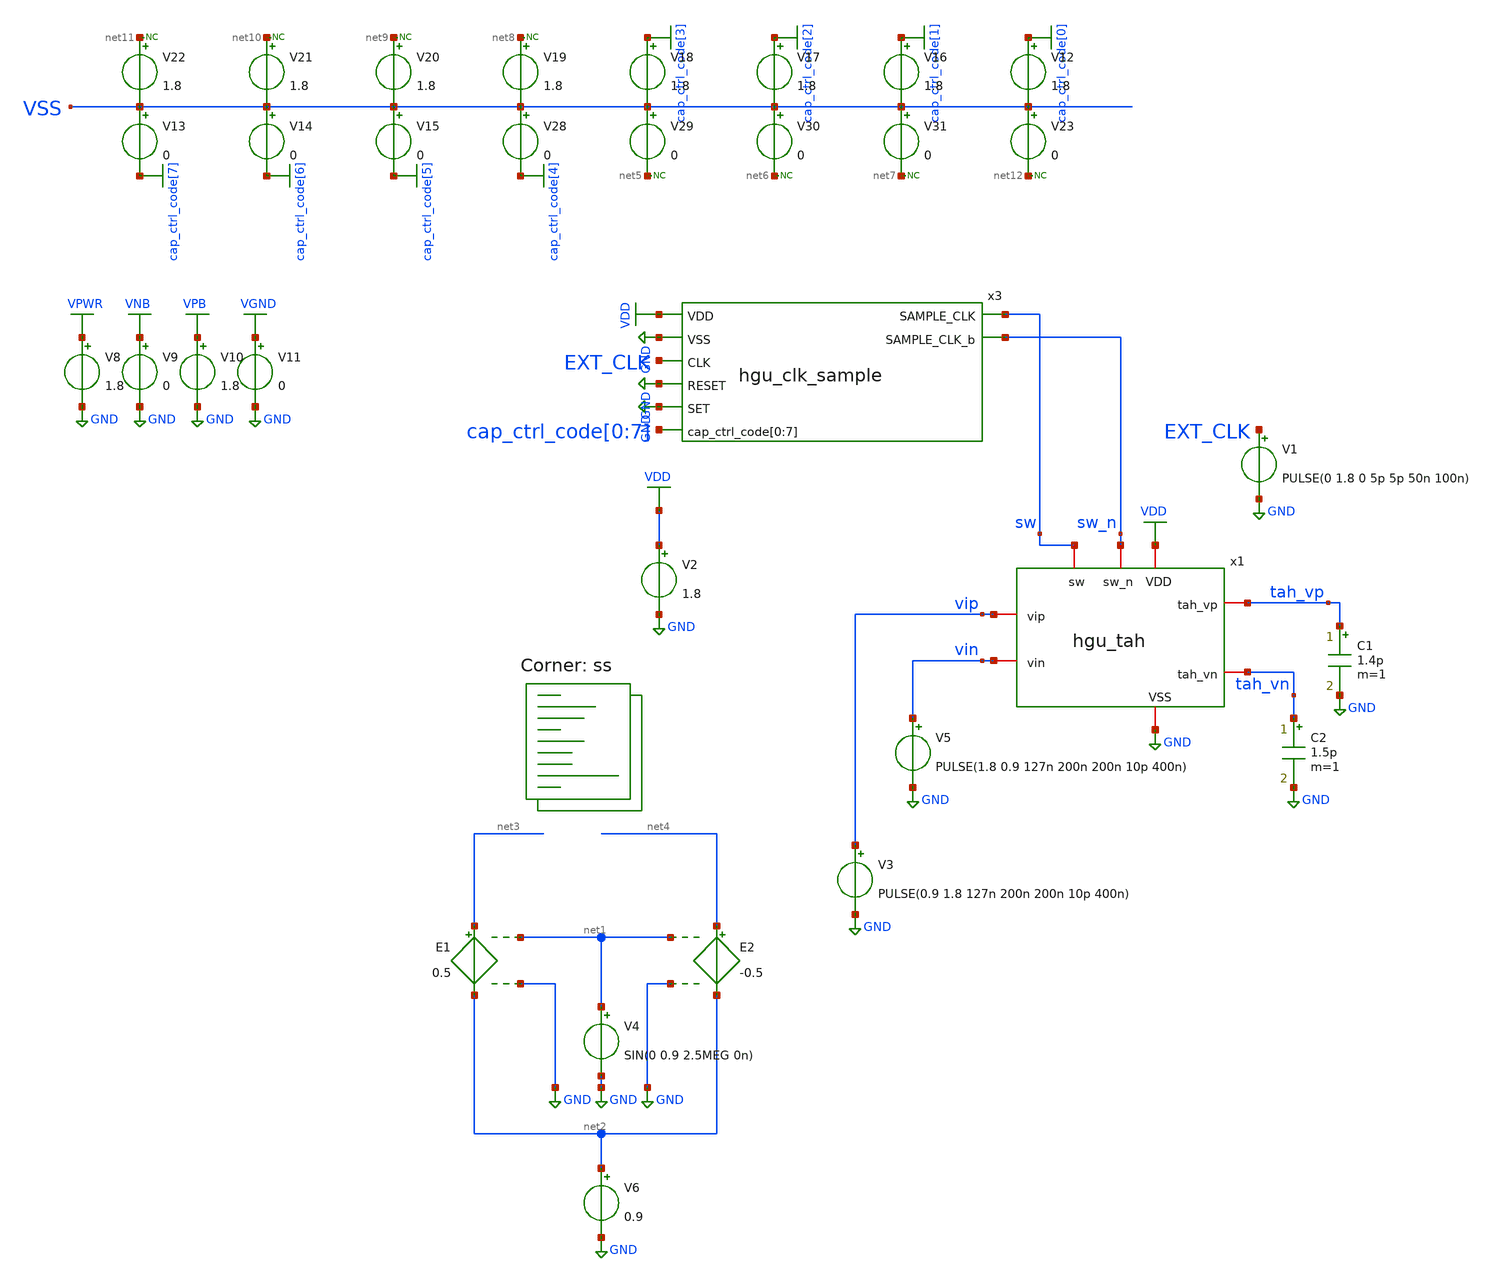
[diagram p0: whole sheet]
** sch_path: hgu/tb/tb_hgu_tah_nonideal.sch
**.subckt tb_hgu_tah_nonideal
x1 sw VDD GND sw_n tah_vp vip vin tah_vn hgu_tah
V2 VDD GND 1.8
C2 tah_vn GND 1.5p m=1
C1 tah_vp GND 1.4p m=1
V1 EXT_CLK GND PULSE(0 1.8 0 5p 5p 50n 100n)
V4 net1 GND SIN(0 0.9 2.5MEG 0n)
E1 net3 net2 net1 GND 0.5
E2 net4 net2 net1 GND -0.5
V6 net2 GND 0.9
x3 sw VDD GND EXT_CLK GND GND sw_n cap_ctrl_code[0] cap_ctrl_code[1] cap_ctrl_code[2]
+ cap_ctrl_code[3] cap_ctrl_code[4] cap_ctrl_code[5] cap_ctrl_code[6] cap_ctrl_code[7] hgu_clk_sample
V12 cap_ctrl_code[0] VSS 1.8
V13 VSS cap_ctrl_code[7] 0
V14 VSS cap_ctrl_code[6] 0
V15 VSS cap_ctrl_code[5] 0
V28 VSS cap_ctrl_code[4] 0
V29 VSS net5 0
V30 VSS net6 0
V31 VSS net7 0
V16 cap_ctrl_code[1] VSS 1.8
V17 cap_ctrl_code[2] VSS 1.8
V18 cap_ctrl_code[3] VSS 1.8
V19 net8 VSS 1.8
V20 net9 VSS 1.8
V21 net10 VSS 1.8
V22 net11 VSS 1.8
V23 VSS net12 0
* noconn #net11
* noconn #net10
* noconn #net9
* noconn #net8
* noconn #net5
* noconn #net6
* noconn #net7
* noconn #net12
V8 VPWR GND 1.8
V9 VNB GND 0
V10 VPB GND 1.8
V11 VGND GND 0
V3 vip GND PULSE(0.9 1.8 127n 200n 200n 10p 400n)
V5 vin GND PULSE(1.8 0.9 127n 200n 200n 10p 400n)
**** begin user architecture code


.save all
.temp = 25
.tran 100p 600n
.OPTIONS savecurrents
.include /foss/pdks/sky130A/libs.ref/sky130_fd_sc_hd/spice/sky130_fd_sc_hd.spice

.control
run
	plot v(sw)-0.9 v(sw_n)-0.9 tah_vp-tah_vn vip-vin
        let svdd = 1.8
        let max = svdd*0.8
        let min = svdd*0.2
        let mid = svdd*0.5
	let input = vip-vin
        meas tran rising_s find time when V(tah_vp-tah_vn)=min RISE=1 TD=100n
        meas tran rising_e find time when V(tah_vp-tah_vn)=max RISE=1 TD=100n
        let rising_time = rising_e-rising_s
        meas tran falling_s find time when V(tah_vp-tah_vn)=max FALL=1 TD=1000p
        meas tran falling_e find time when V(tah_vp-tah_vn)=min FALL=1 TD=1000p
        let falling_time = falling_e-falling_s
        meas tran IN find time when V(sw)=mid RISE=1 TD=350n
        meas tran OUT find time when V(tah_vp-tah_vn)=mid RISE=1 TD=350n
        let rising_delay = OUT-IN
        meas tran fIN find time when V(sw)=mid RISE=1 TD=100n
        meas tran fOUT find time when V(tah_vp-tah_vn)=mid FALL=1 TD=100n
        let falling_delay = fOUT-fIN
	meas tran holdval find input when V(sw)=mid FALL=1 TD=300n


        print holdval

*plot v(sw)+2 v(sw) tah_vp tah_vn+2
*plot v(sw) tah_vp-tah_vn vip-vin
.endc


.lib $::SKYWATER_MODELS/sky130.lib.spice ss
**** end user architecture code
**.ends

* expanding   symbol:  ../xschem/hgu_clk_sample.sym # of pins=8
** sym_path: hgu/xschem/hgu_clk_sample.sym
** sch_path: hgu/xschem/hgu_clk_sample.sch
.subckt hgu_clk_sample SAMPLE_CLK VDD VSS CLK RESET SET SAMPLE_CLK_b cap_ctrl_code[0]
+ cap_ctrl_code[1] cap_ctrl_code[2] cap_ctrl_code[3] cap_ctrl_code[4] cap_ctrl_code[5] cap_ctrl_code[6]
+ cap_ctrl_code[7]
*.ipin VDD
*.ipin VSS
*.ipin SET
*.ipin RESET
*.ipin CLK
*.ipin
*+ cap_ctrl_code[0],cap_ctrl_code[1],cap_ctrl_code[2],cap_ctrl_code[3],cap_ctrl_code[4],cap_ctrl_code[5],cap_ctrl_code[6],cap_ctrl_code[7]
*.opin SAMPLE_CLK
*.opin SAMPLE_CLK_b
x1 net2 CLK RESET SET hgu_clk_div
x2 VDD net2 net8 VSS cap_ctrl_code[0] cap_ctrl_code[1] cap_ctrl_code[2] cap_ctrl_code[3]
+ cap_ctrl_code[4] cap_ctrl_code[5] cap_ctrl_code[6] cap_ctrl_code[7] hgu_delay DELAY_CAP=8f
x7 net8 VGND VNB VPB VPWR net1 sky130_fd_sc_hd__inv_1
C1 net1 VSS 5f m=1
C2 net2 VSS 5f m=1
C3 net8 VSS 5f m=1
x3 net2 net1 VGND VNB VPB VPWR net4 sky130_fd_sc_hd__nand2_1
XM7 net7 net3 VSS VSS sky130_fd_pr__nfet_01v8 L=0.15 W=0.42 nf=1 ad='int((nf+1)/2) * W/nf * 0.29' as='int((nf+2)/2) * W/nf * 0.29'
+ pd='2*int((nf+1)/2) * (W/nf + 0.29)' ps='2*int((nf+2)/2) * (W/nf + 0.29)' nrd='0.29 / W' nrs='0.29 / W'
+ sa=0 sb=0 sd=0 mult=1 m=1
XM8 net7 net3 VDD VDD sky130_fd_pr__pfet_01v8 L=0.15 W=1.26 nf=1 ad='int((nf+1)/2) * W/nf * 0.29' as='int((nf+2)/2) * W/nf * 0.29'
+ pd='2*int((nf+1)/2) * (W/nf + 0.29)' ps='2*int((nf+2)/2) * (W/nf + 0.29)' nrd='0.29 / W' nrs='0.29 / W'
+ sa=0 sb=0 sd=0 mult=1 m=1
XM9 net5 net4 VSS VSS sky130_fd_pr__nfet_01v8 L=0.15 W=0.42 nf=1 ad='int((nf+1)/2) * W/nf * 0.29' as='int((nf+2)/2) * W/nf * 0.29'
+ pd='2*int((nf+1)/2) * (W/nf + 0.29)' ps='2*int((nf+2)/2) * (W/nf + 0.29)' nrd='0.29 / W' nrs='0.29 / W'
+ sa=0 sb=0 sd=0 mult=1 m=1
XM10 net5 net4 VDD VDD sky130_fd_pr__pfet_01v8 L=0.15 W=1.4 nf=1 ad='int((nf+1)/2) * W/nf * 0.29' as='int((nf+2)/2) * W/nf * 0.29'
+ pd='2*int((nf+1)/2) * (W/nf + 0.29)' ps='2*int((nf+2)/2) * (W/nf + 0.29)' nrd='0.29 / W' nrs='0.29 / W'
+ sa=0 sb=0 sd=0 mult=1 m=1
XM11 net6 net5 VSS VSS sky130_fd_pr__nfet_01v8 L=0.15 W=0.42 nf=1 ad='int((nf+1)/2) * W/nf * 0.29' as='int((nf+2)/2) * W/nf * 0.29'
+ pd='2*int((nf+1)/2) * (W/nf + 0.29)' ps='2*int((nf+2)/2) * (W/nf + 0.29)' nrd='0.29 / W' nrs='0.29 / W'
+ sa=0 sb=0 sd=0 mult=1 m=1
XM12 net6 net5 VDD VDD sky130_fd_pr__pfet_01v8 L=0.15 W=1.26 nf=1 ad='int((nf+1)/2) * W/nf * 0.29' as='int((nf+2)/2) * W/nf * 0.29'
+ pd='2*int((nf+1)/2) * (W/nf + 0.29)' ps='2*int((nf+2)/2) * (W/nf + 0.29)' nrd='0.29 / W' nrs='0.29 / W'
+ sa=0 sb=0 sd=0 mult=1 m=1
XM13 net4 VSS net3 VDD sky130_fd_pr__pfet_01v8 L=0.15 W=1.9 nf=1 ad='int((nf+1)/2) * W/nf * 0.29' as='int((nf+2)/2) * W/nf * 0.29'
+ pd='2*int((nf+1)/2) * (W/nf + 0.29)' ps='2*int((nf+2)/2) * (W/nf + 0.29)' nrd='0.29 / W' nrs='0.29 / W'
+ sa=0 sb=0 sd=0 mult=1 m=1
XM14 net4 VDD net3 VSS sky130_fd_pr__nfet_01v8 L=0.15 W=0.42 nf=1 ad='int((nf+1)/2) * W/nf * 0.29' as='int((nf+2)/2) * W/nf * 0.29'
+ pd='2*int((nf+1)/2) * (W/nf + 0.29)' ps='2*int((nf+2)/2) * (W/nf + 0.29)' nrd='0.29 / W' nrs='0.29 / W'
+ sa=0 sb=0 sd=0 mult=1 m=1
XM15 SAMPLE_CLK net6 VSS VSS sky130_fd_pr__nfet_01v8 L=0.15 W='0.42 * 3 ' nf=3 ad='int((nf+1)/2) * W / nf * 0.29'
+ as='int((nf+2)/2) * W / nf * 0.29' pd='2*int((nf+1)/2) * (W / nf + 0.29)' ps='2*int((nf+2)/2) * (W / nf + 0.29)'
+ nrd='0.29 / W ' nrs='0.29 / W ' sa=0 sb=0 sd=0 mult=1 m=1
XM16 SAMPLE_CLK net6 VDD VDD sky130_fd_pr__pfet_01v8 L=0.15 W='1.26 * 3 ' nf=3 ad='int((nf+1)/2) * W / nf * 0.29'
+ as='int((nf+2)/2) * W / nf * 0.29' pd='2*int((nf+1)/2) * (W / nf + 0.29)' ps='2*int((nf+2)/2) * (W / nf + 0.29)'
+ nrd='0.29 / W ' nrs='0.29 / W ' sa=0 sb=0 sd=0 mult=1 m=1
XM17 SAMPLE_CLK_b net7 VDD VDD sky130_fd_pr__pfet_01v8 L=0.15 W='1.26 * 3 ' nf=3 ad='int((nf+1)/2) * W / nf * 0.29'
+ as='int((nf+2)/2) * W / nf * 0.29' pd='2*int((nf+1)/2) * (W / nf + 0.29)' ps='2*int((nf+2)/2) * (W / nf + 0.29)'
+ nrd='0.29 / W ' nrs='0.29 / W ' sa=0 sb=0 sd=0 mult=1 m=1
XM18 SAMPLE_CLK_b net7 VSS VSS sky130_fd_pr__nfet_01v8 L=0.15 W='0.42 * 3 ' nf=3 ad='int((nf+1)/2) * W / nf * 0.29'
+ as='int((nf+2)/2) * W / nf * 0.29' pd='2*int((nf+1)/2) * (W / nf + 0.29)' ps='2*int((nf+2)/2) * (W / nf + 0.29)'
+ nrd='0.29 / W ' nrs='0.29 / W ' sa=0 sb=0 sd=0 mult=1 m=1
.ends


* expanding   symbol:  ../xschem/hgu_clk_div.sym # of pins=4
** sym_path: hgu/xschem/hgu_clk_div.sym
** sch_path: hgu/xschem/hgu_clk_div.sch
.subckt hgu_clk_div DIV_CLK CLK RESET SET
*.opin DIV_CLK
*.ipin SET
*.ipin RESET
*.ipin CLK
x2 CLK D_loop net1 net2 VGND VNB VPB VPWR DIV_CLK D_loop sky130_fd_sc_hd__dfbbp_1
x3 SET VGND VNB VPB VPWR net2 sky130_fd_sc_hd__inv_1
x4 RESET VGND VNB VPB VPWR net1 sky130_fd_sc_hd__inv_1
.ends


* expanding   symbol:  ../xschem/hgu_delay.sym # of pins=5
** sym_path: hgu/xschem/hgu_delay.sym
** sch_path: hgu/xschem/hgu_delay.sch
.subckt hgu_delay VDD IN OUT VSS CAP_CTRL_CODE[0] CAP_CTRL_CODE[1] CAP_CTRL_CODE[2] CAP_CTRL_CODE[3]
+ CAP_CTRL_CODE[4] CAP_CTRL_CODE[5] CAP_CTRL_CODE[6] CAP_CTRL_CODE[7]  DELAY_CAP=DELAY_CAP
*.ipin IN
*.ipin VDD
*.ipin VSS
*.opin OUT
*.ipin
*+ CAP_CTRL_CODE[0],CAP_CTRL_CODE[1],CAP_CTRL_CODE[2],CAP_CTRL_CODE[3],CAP_CTRL_CODE[4],CAP_CTRL_CODE[5],CAP_CTRL_CODE[6],CAP_CTRL_CODE[7]
XM1 net1 IN VSS VSS sky130_fd_pr__nfet_01v8 L=3.69 W=0.42 nf=1 ad='int((nf+1)/2) * W/nf * 0.29' as='int((nf+2)/2) * W/nf * 0.29'
+ pd='2*int((nf+1)/2) * (W/nf + 0.29)' ps='2*int((nf+2)/2) * (W/nf + 0.29)' nrd='0.29 / W' nrs='0.29 / W'
+ sa=0 sb=0 sd=0 mult=1 m=1
XM2 net1 IN VDD VDD sky130_fd_pr__pfet_01v8 L=1.5 W=0.8 nf=1 ad='int((nf+1)/2) * W/nf * 0.29' as='int((nf+2)/2) * W/nf * 0.29'
+ pd='2*int((nf+1)/2) * (W/nf + 0.29)' ps='2*int((nf+2)/2) * (W/nf + 0.29)' nrd='0.29 / W' nrs='0.29 / W'
+ sa=0 sb=0 sd=0 mult=1 m=1
XM3 VSS net1 VSS VSS sky130_fd_pr__nfet_01v8 L=2.045 W=1.375 nf=1 ad='int((nf+1)/2) * W/nf * 0.29' as='int((nf+2)/2) * W/nf * 0.29'
+ pd='2*int((nf+1)/2) * (W/nf + 0.29)' ps='2*int((nf+2)/2) * (W/nf + 0.29)' nrd='0.29 / W' nrs='0.29 / W'
+ sa=0 sb=0 sd=0 mult=1 m=1
XM4 OUT net1 net3 VSS sky130_fd_pr__nfet_01v8 L=0.15 W=0.42 nf=1 ad='int((nf+1)/2) * W/nf * 0.29' as='int((nf+2)/2) * W/nf * 0.29'
+ pd='2*int((nf+1)/2) * (W/nf + 0.29)' ps='2*int((nf+2)/2) * (W/nf + 0.29)' nrd='0.29 / W' nrs='0.29 / W'
+ sa=0 sb=0 sd=0 mult=1 m=1
XM5 OUT net1 net2 VDD sky130_fd_pr__pfet_01v8 L=0.15 W=0.8 nf=1 ad='int((nf+1)/2) * W/nf * 0.29' as='int((nf+2)/2) * W/nf * 0.29'
+ pd='2*int((nf+1)/2) * (W/nf + 0.29)' ps='2*int((nf+2)/2) * (W/nf + 0.29)' nrd='0.29 / W' nrs='0.29 / W'
+ sa=0 sb=0 sd=0 mult=1 m=1
XM6 net3 net1 VSS VSS sky130_fd_pr__nfet_01v8 L=0.15 W=0.42 nf=1 ad='int((nf+1)/2) * W/nf * 0.29' as='int((nf+2)/2) * W/nf * 0.29'
+ pd='2*int((nf+1)/2) * (W/nf + 0.29)' ps='2*int((nf+2)/2) * (W/nf + 0.29)' nrd='0.29 / W' nrs='0.29 / W'
+ sa=0 sb=0 sd=0 mult=1 m=1
XM7 net2 net1 VDD VDD sky130_fd_pr__pfet_01v8 L=0.15 W=0.8 nf=1 ad='int((nf+1)/2) * W/nf * 0.29' as='int((nf+2)/2) * W/nf * 0.29'
+ pd='2*int((nf+1)/2) * (W/nf + 0.29)' ps='2*int((nf+2)/2) * (W/nf + 0.29)' nrd='0.29 / W' nrs='0.29 / W'
+ sa=0 sb=0 sd=0 mult=1 m=1
XM8 VDD OUT net3 VSS sky130_fd_pr__nfet_01v8 L=0.15 W=0.84 nf=1 ad='int((nf+1)/2) * W/nf * 0.29' as='int((nf+2)/2) * W/nf * 0.29'
+ pd='2*int((nf+1)/2) * (W/nf + 0.29)' ps='2*int((nf+2)/2) * (W/nf + 0.29)' nrd='0.29 / W' nrs='0.29 / W'
+ sa=0 sb=0 sd=0 mult=1 m=1
XM9 VSS OUT net2 VDD sky130_fd_pr__pfet_01v8 L=0.15 W=1.6 nf=1 ad='int((nf+1)/2) * W/nf * 0.29' as='int((nf+2)/2) * W/nf * 0.29'
+ pd='2*int((nf+1)/2) * (W/nf + 0.29)' ps='2*int((nf+2)/2) * (W/nf + 0.29)' nrd='0.29 / W' nrs='0.29 / W'
+ sa=0 sb=0 sd=0 mult=1 m=1
x2 CAP_CTRL_CODE[0] VSS net1 hgu_sw_cap DELAY_CAP=DELAY_CAP
x3[1] CAP_CTRL_CODE[1] VSS net1 hgu_sw_cap DELAY_CAP=DELAY_CAP
x3[0] CAP_CTRL_CODE[1] VSS net1 hgu_sw_cap DELAY_CAP=DELAY_CAP
x4[3] CAP_CTRL_CODE[2] VSS net1 hgu_sw_cap DELAY_CAP=DELAY_CAP
x4[2] CAP_CTRL_CODE[2] VSS net1 hgu_sw_cap DELAY_CAP=DELAY_CAP
x4[1] CAP_CTRL_CODE[2] VSS net1 hgu_sw_cap DELAY_CAP=DELAY_CAP
x4[0] CAP_CTRL_CODE[2] VSS net1 hgu_sw_cap DELAY_CAP=DELAY_CAP
x5[7] CAP_CTRL_CODE[3] VSS net1 hgu_sw_cap DELAY_CAP=DELAY_CAP
x5[6] CAP_CTRL_CODE[3] VSS net1 hgu_sw_cap DELAY_CAP=DELAY_CAP
x5[5] CAP_CTRL_CODE[3] VSS net1 hgu_sw_cap DELAY_CAP=DELAY_CAP
x5[4] CAP_CTRL_CODE[3] VSS net1 hgu_sw_cap DELAY_CAP=DELAY_CAP
x5[3] CAP_CTRL_CODE[3] VSS net1 hgu_sw_cap DELAY_CAP=DELAY_CAP
x5[2] CAP_CTRL_CODE[3] VSS net1 hgu_sw_cap DELAY_CAP=DELAY_CAP
x5[1] CAP_CTRL_CODE[3] VSS net1 hgu_sw_cap DELAY_CAP=DELAY_CAP
x5[0] CAP_CTRL_CODE[3] VSS net1 hgu_sw_cap DELAY_CAP=DELAY_CAP
x6[15] CAP_CTRL_CODE[4] VSS net1 hgu_sw_cap DELAY_CAP=DELAY_CAP
x6[14] CAP_CTRL_CODE[4] VSS net1 hgu_sw_cap DELAY_CAP=DELAY_CAP
x6[13] CAP_CTRL_CODE[4] VSS net1 hgu_sw_cap DELAY_CAP=DELAY_CAP
x6[12] CAP_CTRL_CODE[4] VSS net1 hgu_sw_cap DELAY_CAP=DELAY_CAP
x6[11] CAP_CTRL_CODE[4] VSS net1 hgu_sw_cap DELAY_CAP=DELAY_CAP
x6[10] CAP_CTRL_CODE[4] VSS net1 hgu_sw_cap DELAY_CAP=DELAY_CAP
x6[9] CAP_CTRL_CODE[4] VSS net1 hgu_sw_cap DELAY_CAP=DELAY_CAP
x6[8] CAP_CTRL_CODE[4] VSS net1 hgu_sw_cap DELAY_CAP=DELAY_CAP
x6[7] CAP_CTRL_CODE[4] VSS net1 hgu_sw_cap DELAY_CAP=DELAY_CAP
x6[6] CAP_CTRL_CODE[4] VSS net1 hgu_sw_cap DELAY_CAP=DELAY_CAP
x6[5] CAP_CTRL_CODE[4] VSS net1 hgu_sw_cap DELAY_CAP=DELAY_CAP
x6[4] CAP_CTRL_CODE[4] VSS net1 hgu_sw_cap DELAY_CAP=DELAY_CAP
x6[3] CAP_CTRL_CODE[4] VSS net1 hgu_sw_cap DELAY_CAP=DELAY_CAP
x6[2] CAP_CTRL_CODE[4] VSS net1 hgu_sw_cap DELAY_CAP=DELAY_CAP
x6[1] CAP_CTRL_CODE[4] VSS net1 hgu_sw_cap DELAY_CAP=DELAY_CAP
x6[0] CAP_CTRL_CODE[4] VSS net1 hgu_sw_cap DELAY_CAP=DELAY_CAP
x7[31] CAP_CTRL_CODE[5] VSS net1 hgu_sw_cap DELAY_CAP=DELAY_CAP
x7[30] CAP_CTRL_CODE[5] VSS net1 hgu_sw_cap DELAY_CAP=DELAY_CAP
x7[29] CAP_CTRL_CODE[5] VSS net1 hgu_sw_cap DELAY_CAP=DELAY_CAP
x7[28] CAP_CTRL_CODE[5] VSS net1 hgu_sw_cap DELAY_CAP=DELAY_CAP
x7[27] CAP_CTRL_CODE[5] VSS net1 hgu_sw_cap DELAY_CAP=DELAY_CAP
x7[26] CAP_CTRL_CODE[5] VSS net1 hgu_sw_cap DELAY_CAP=DELAY_CAP
x7[25] CAP_CTRL_CODE[5] VSS net1 hgu_sw_cap DELAY_CAP=DELAY_CAP
x7[24] CAP_CTRL_CODE[5] VSS net1 hgu_sw_cap DELAY_CAP=DELAY_CAP
x7[23] CAP_CTRL_CODE[5] VSS net1 hgu_sw_cap DELAY_CAP=DELAY_CAP
x7[22] CAP_CTRL_CODE[5] VSS net1 hgu_sw_cap DELAY_CAP=DELAY_CAP
x7[21] CAP_CTRL_CODE[5] VSS net1 hgu_sw_cap DELAY_CAP=DELAY_CAP
x7[20] CAP_CTRL_CODE[5] VSS net1 hgu_sw_cap DELAY_CAP=DELAY_CAP
x7[19] CAP_CTRL_CODE[5] VSS net1 hgu_sw_cap DELAY_CAP=DELAY_CAP
x7[18] CAP_CTRL_CODE[5] VSS net1 hgu_sw_cap DELAY_CAP=DELAY_CAP
x7[17] CAP_CTRL_CODE[5] VSS net1 hgu_sw_cap DELAY_CAP=DELAY_CAP
x7[16] CAP_CTRL_CODE[5] VSS net1 hgu_sw_cap DELAY_CAP=DELAY_CAP
x7[15] CAP_CTRL_CODE[5] VSS net1 hgu_sw_cap DELAY_CAP=DELAY_CAP
x7[14] CAP_CTRL_CODE[5] VSS net1 hgu_sw_cap DELAY_CAP=DELAY_CAP
x7[13] CAP_CTRL_CODE[5] VSS net1 hgu_sw_cap DELAY_CAP=DELAY_CAP
x7[12] CAP_CTRL_CODE[5] VSS net1 hgu_sw_cap DELAY_CAP=DELAY_CAP
x7[11] CAP_CTRL_CODE[5] VSS net1 hgu_sw_cap DELAY_CAP=DELAY_CAP
x7[10] CAP_CTRL_CODE[5] VSS net1 hgu_sw_cap DELAY_CAP=DELAY_CAP
x7[9] CAP_CTRL_CODE[5] VSS net1 hgu_sw_cap DELAY_CAP=DELAY_CAP
x7[8] CAP_CTRL_CODE[5] VSS net1 hgu_sw_cap DELAY_CAP=DELAY_CAP
x7[7] CAP_CTRL_CODE[5] VSS net1 hgu_sw_cap DELAY_CAP=DELAY_CAP
x7[6] CAP_CTRL_CODE[5] VSS net1 hgu_sw_cap DELAY_CAP=DELAY_CAP
x7[5] CAP_CTRL_CODE[5] VSS net1 hgu_sw_cap DELAY_CAP=DELAY_CAP
x7[4] CAP_CTRL_CODE[5] VSS net1 hgu_sw_cap DELAY_CAP=DELAY_CAP
x7[3] CAP_CTRL_CODE[5] VSS net1 hgu_sw_cap DELAY_CAP=DELAY_CAP
x7[2] CAP_CTRL_CODE[5] VSS net1 hgu_sw_cap DELAY_CAP=DELAY_CAP
x7[1] CAP_CTRL_CODE[5] VSS net1 hgu_sw_cap DELAY_CAP=DELAY_CAP
x7[0] CAP_CTRL_CODE[5] VSS net1 hgu_sw_cap DELAY_CAP=DELAY_CAP
x8[63] CAP_CTRL_CODE[6] VSS net1 hgu_sw_cap DELAY_CAP=DELAY_CAP
x8[62] CAP_CTRL_CODE[6] VSS net1 hgu_sw_cap DELAY_CAP=DELAY_CAP
x8[61] CAP_CTRL_CODE[6] VSS net1 hgu_sw_cap DELAY_CAP=DELAY_CAP
x8[60] CAP_CTRL_CODE[6] VSS net1 hgu_sw_cap DELAY_CAP=DELAY_CAP
x8[59] CAP_CTRL_CODE[6] VSS net1 hgu_sw_cap DELAY_CAP=DELAY_CAP
x8[58] CAP_CTRL_CODE[6] VSS net1 hgu_sw_cap DELAY_CAP=DELAY_CAP
x8[57] CAP_CTRL_CODE[6] VSS net1 hgu_sw_cap DELAY_CAP=DELAY_CAP
x8[56] CAP_CTRL_CODE[6] VSS net1 hgu_sw_cap DELAY_CAP=DELAY_CAP
x8[55] CAP_CTRL_CODE[6] VSS net1 hgu_sw_cap DELAY_CAP=DELAY_CAP
x8[54] CAP_CTRL_CODE[6] VSS net1 hgu_sw_cap DELAY_CAP=DELAY_CAP
x8[53] CAP_CTRL_CODE[6] VSS net1 hgu_sw_cap DELAY_CAP=DELAY_CAP
x8[52] CAP_CTRL_CODE[6] VSS net1 hgu_sw_cap DELAY_CAP=DELAY_CAP
x8[51] CAP_CTRL_CODE[6] VSS net1 hgu_sw_cap DELAY_CAP=DELAY_CAP
x8[50] CAP_CTRL_CODE[6] VSS net1 hgu_sw_cap DELAY_CAP=DELAY_CAP
x8[49] CAP_CTRL_CODE[6] VSS net1 hgu_sw_cap DELAY_CAP=DELAY_CAP
x8[48] CAP_CTRL_CODE[6] VSS net1 hgu_sw_cap DELAY_CAP=DELAY_CAP
x8[47] CAP_CTRL_CODE[6] VSS net1 hgu_sw_cap DELAY_CAP=DELAY_CAP
x8[46] CAP_CTRL_CODE[6] VSS net1 hgu_sw_cap DELAY_CAP=DELAY_CAP
x8[45] CAP_CTRL_CODE[6] VSS net1 hgu_sw_cap DELAY_CAP=DELAY_CAP
x8[44] CAP_CTRL_CODE[6] VSS net1 hgu_sw_cap DELAY_CAP=DELAY_CAP
x8[43] CAP_CTRL_CODE[6] VSS net1 hgu_sw_cap DELAY_CAP=DELAY_CAP
x8[42] CAP_CTRL_CODE[6] VSS net1 hgu_sw_cap DELAY_CAP=DELAY_CAP
x8[41] CAP_CTRL_CODE[6] VSS net1 hgu_sw_cap DELAY_CAP=DELAY_CAP
x8[40] CAP_CTRL_CODE[6] VSS net1 hgu_sw_cap DELAY_CAP=DELAY_CAP
x8[39] CAP_CTRL_CODE[6] VSS net1 hgu_sw_cap DELAY_CAP=DELAY_CAP
x8[38] CAP_CTRL_CODE[6] VSS net1 hgu_sw_cap DELAY_CAP=DELAY_CAP
x8[37] CAP_CTRL_CODE[6] VSS net1 hgu_sw_cap DELAY_CAP=DELAY_CAP
x8[36] CAP_CTRL_CODE[6] VSS net1 hgu_sw_cap DELAY_CAP=DELAY_CAP
x8[35] CAP_CTRL_CODE[6] VSS net1 hgu_sw_cap DELAY_CAP=DELAY_CAP
x8[34] CAP_CTRL_CODE[6] VSS net1 hgu_sw_cap DELAY_CAP=DELAY_CAP
x8[33] CAP_CTRL_CODE[6] VSS net1 hgu_sw_cap DELAY_CAP=DELAY_CAP
x8[32] CAP_CTRL_CODE[6] VSS net1 hgu_sw_cap DELAY_CAP=DELAY_CAP
x8[31] CAP_CTRL_CODE[6] VSS net1 hgu_sw_cap DELAY_CAP=DELAY_CAP
x8[30] CAP_CTRL_CODE[6] VSS net1 hgu_sw_cap DELAY_CAP=DELAY_CAP
x8[29] CAP_CTRL_CODE[6] VSS net1 hgu_sw_cap DELAY_CAP=DELAY_CAP
x8[28] CAP_CTRL_CODE[6] VSS net1 hgu_sw_cap DELAY_CAP=DELAY_CAP
x8[27] CAP_CTRL_CODE[6] VSS net1 hgu_sw_cap DELAY_CAP=DELAY_CAP
x8[26] CAP_CTRL_CODE[6] VSS net1 hgu_sw_cap DELAY_CAP=DELAY_CAP
x8[25] CAP_CTRL_CODE[6] VSS net1 hgu_sw_cap DELAY_CAP=DELAY_CAP
x8[24] CAP_CTRL_CODE[6] VSS net1 hgu_sw_cap DELAY_CAP=DELAY_CAP
x8[23] CAP_CTRL_CODE[6] VSS net1 hgu_sw_cap DELAY_CAP=DELAY_CAP
x8[22] CAP_CTRL_CODE[6] VSS net1 hgu_sw_cap DELAY_CAP=DELAY_CAP
x8[21] CAP_CTRL_CODE[6] VSS net1 hgu_sw_cap DELAY_CAP=DELAY_CAP
x8[20] CAP_CTRL_CODE[6] VSS net1 hgu_sw_cap DELAY_CAP=DELAY_CAP
x8[19] CAP_CTRL_CODE[6] VSS net1 hgu_sw_cap DELAY_CAP=DELAY_CAP
x8[18] CAP_CTRL_CODE[6] VSS net1 hgu_sw_cap DELAY_CAP=DELAY_CAP
x8[17] CAP_CTRL_CODE[6] VSS net1 hgu_sw_cap DELAY_CAP=DELAY_CAP
x8[16] CAP_CTRL_CODE[6] VSS net1 hgu_sw_cap DELAY_CAP=DELAY_CAP
x8[15] CAP_CTRL_CODE[6] VSS net1 hgu_sw_cap DELAY_CAP=DELAY_CAP
x8[14] CAP_CTRL_CODE[6] VSS net1 hgu_sw_cap DELAY_CAP=DELAY_CAP
x8[13] CAP_CTRL_CODE[6] VSS net1 hgu_sw_cap DELAY_CAP=DELAY_CAP
x8[12] CAP_CTRL_CODE[6] VSS net1 hgu_sw_cap DELAY_CAP=DELAY_CAP
x8[11] CAP_CTRL_CODE[6] VSS net1 hgu_sw_cap DELAY_CAP=DELAY_CAP
x8[10] CAP_CTRL_CODE[6] VSS net1 hgu_sw_cap DELAY_CAP=DELAY_CAP
x8[9] CAP_CTRL_CODE[6] VSS net1 hgu_sw_cap DELAY_CAP=DELAY_CAP
x8[8] CAP_CTRL_CODE[6] VSS net1 hgu_sw_cap DELAY_CAP=DELAY_CAP
x8[7] CAP_CTRL_CODE[6] VSS net1 hgu_sw_cap DELAY_CAP=DELAY_CAP
x8[6] CAP_CTRL_CODE[6] VSS net1 hgu_sw_cap DELAY_CAP=DELAY_CAP
x8[5] CAP_CTRL_CODE[6] VSS net1 hgu_sw_cap DELAY_CAP=DELAY_CAP
x8[4] CAP_CTRL_CODE[6] VSS net1 hgu_sw_cap DELAY_CAP=DELAY_CAP
x8[3] CAP_CTRL_CODE[6] VSS net1 hgu_sw_cap DELAY_CAP=DELAY_CAP
x8[2] CAP_CTRL_CODE[6] VSS net1 hgu_sw_cap DELAY_CAP=DELAY_CAP
x8[1] CAP_CTRL_CODE[6] VSS net1 hgu_sw_cap DELAY_CAP=DELAY_CAP
x8[0] CAP_CTRL_CODE[6] VSS net1 hgu_sw_cap DELAY_CAP=DELAY_CAP
x1[127] CAP_CTRL_CODE[7] VSS net1 hgu_sw_cap DELAY_CAP=DELAY_CAP
x1[126] CAP_CTRL_CODE[7] VSS net1 hgu_sw_cap DELAY_CAP=DELAY_CAP
x1[125] CAP_CTRL_CODE[7] VSS net1 hgu_sw_cap DELAY_CAP=DELAY_CAP
x1[124] CAP_CTRL_CODE[7] VSS net1 hgu_sw_cap DELAY_CAP=DELAY_CAP
x1[123] CAP_CTRL_CODE[7] VSS net1 hgu_sw_cap DELAY_CAP=DELAY_CAP
x1[122] CAP_CTRL_CODE[7] VSS net1 hgu_sw_cap DELAY_CAP=DELAY_CAP
x1[121] CAP_CTRL_CODE[7] VSS net1 hgu_sw_cap DELAY_CAP=DELAY_CAP
x1[120] CAP_CTRL_CODE[7] VSS net1 hgu_sw_cap DELAY_CAP=DELAY_CAP
x1[119] CAP_CTRL_CODE[7] VSS net1 hgu_sw_cap DELAY_CAP=DELAY_CAP
x1[118] CAP_CTRL_CODE[7] VSS net1 hgu_sw_cap DELAY_CAP=DELAY_CAP
x1[117] CAP_CTRL_CODE[7] VSS net1 hgu_sw_cap DELAY_CAP=DELAY_CAP
x1[116] CAP_CTRL_CODE[7] VSS net1 hgu_sw_cap DELAY_CAP=DELAY_CAP
x1[115] CAP_CTRL_CODE[7] VSS net1 hgu_sw_cap DELAY_CAP=DELAY_CAP
x1[114] CAP_CTRL_CODE[7] VSS net1 hgu_sw_cap DELAY_CAP=DELAY_CAP
x1[113] CAP_CTRL_CODE[7] VSS net1 hgu_sw_cap DELAY_CAP=DELAY_CAP
x1[112] CAP_CTRL_CODE[7] VSS net1 hgu_sw_cap DELAY_CAP=DELAY_CAP
x1[111] CAP_CTRL_CODE[7] VSS net1 hgu_sw_cap DELAY_CAP=DELAY_CAP
x1[110] CAP_CTRL_CODE[7] VSS net1 hgu_sw_cap DELAY_CAP=DELAY_CAP
x1[109] CAP_CTRL_CODE[7] VSS net1 hgu_sw_cap DELAY_CAP=DELAY_CAP
x1[108] CAP_CTRL_CODE[7] VSS net1 hgu_sw_cap DELAY_CAP=DELAY_CAP
x1[107] CAP_CTRL_CODE[7] VSS net1 hgu_sw_cap DELAY_CAP=DELAY_CAP
x1[106] CAP_CTRL_CODE[7] VSS net1 hgu_sw_cap DELAY_CAP=DELAY_CAP
x1[105] CAP_CTRL_CODE[7] VSS net1 hgu_sw_cap DELAY_CAP=DELAY_CAP
x1[104] CAP_CTRL_CODE[7] VSS net1 hgu_sw_cap DELAY_CAP=DELAY_CAP
x1[103] CAP_CTRL_CODE[7] VSS net1 hgu_sw_cap DELAY_CAP=DELAY_CAP
x1[102] CAP_CTRL_CODE[7] VSS net1 hgu_sw_cap DELAY_CAP=DELAY_CAP
x1[101] CAP_CTRL_CODE[7] VSS net1 hgu_sw_cap DELAY_CAP=DELAY_CAP
x1[100] CAP_CTRL_CODE[7] VSS net1 hgu_sw_cap DELAY_CAP=DELAY_CAP
x1[99] CAP_CTRL_CODE[7] VSS net1 hgu_sw_cap DELAY_CAP=DELAY_CAP
x1[98] CAP_CTRL_CODE[7] VSS net1 hgu_sw_cap DELAY_CAP=DELAY_CAP
x1[97] CAP_CTRL_CODE[7] VSS net1 hgu_sw_cap DELAY_CAP=DELAY_CAP
x1[96] CAP_CTRL_CODE[7] VSS net1 hgu_sw_cap DELAY_CAP=DELAY_CAP
x1[95] CAP_CTRL_CODE[7] VSS net1 hgu_sw_cap DELAY_CAP=DELAY_CAP
x1[94] CAP_CTRL_CODE[7] VSS net1 hgu_sw_cap DELAY_CAP=DELAY_CAP
x1[93] CAP_CTRL_CODE[7] VSS net1 hgu_sw_cap DELAY_CAP=DELAY_CAP
x1[92] CAP_CTRL_CODE[7] VSS net1 hgu_sw_cap DELAY_CAP=DELAY_CAP
x1[91] CAP_CTRL_CODE[7] VSS net1 hgu_sw_cap DELAY_CAP=DELAY_CAP
x1[90] CAP_CTRL_CODE[7] VSS net1 hgu_sw_cap DELAY_CAP=DELAY_CAP
x1[89] CAP_CTRL_CODE[7] VSS net1 hgu_sw_cap DELAY_CAP=DELAY_CAP
x1[88] CAP_CTRL_CODE[7] VSS net1 hgu_sw_cap DELAY_CAP=DELAY_CAP
x1[87] CAP_CTRL_CODE[7] VSS net1 hgu_sw_cap DELAY_CAP=DELAY_CAP
x1[86] CAP_CTRL_CODE[7] VSS net1 hgu_sw_cap DELAY_CAP=DELAY_CAP
x1[85] CAP_CTRL_CODE[7] VSS net1 hgu_sw_cap DELAY_CAP=DELAY_CAP
x1[84] CAP_CTRL_CODE[7] VSS net1 hgu_sw_cap DELAY_CAP=DELAY_CAP
x1[83] CAP_CTRL_CODE[7] VSS net1 hgu_sw_cap DELAY_CAP=DELAY_CAP
x1[82] CAP_CTRL_CODE[7] VSS net1 hgu_sw_cap DELAY_CAP=DELAY_CAP
x1[81] CAP_CTRL_CODE[7] VSS net1 hgu_sw_cap DELAY_CAP=DELAY_CAP
x1[80] CAP_CTRL_CODE[7] VSS net1 hgu_sw_cap DELAY_CAP=DELAY_CAP
x1[79] CAP_CTRL_CODE[7] VSS net1 hgu_sw_cap DELAY_CAP=DELAY_CAP
x1[78] CAP_CTRL_CODE[7] VSS net1 hgu_sw_cap DELAY_CAP=DELAY_CAP
x1[77] CAP_CTRL_CODE[7] VSS net1 hgu_sw_cap DELAY_CAP=DELAY_CAP
x1[76] CAP_CTRL_CODE[7] VSS net1 hgu_sw_cap DELAY_CAP=DELAY_CAP
x1[75] CAP_CTRL_CODE[7] VSS net1 hgu_sw_cap DELAY_CAP=DELAY_CAP
x1[74] CAP_CTRL_CODE[7] VSS net1 hgu_sw_cap DELAY_CAP=DELAY_CAP
x1[73] CAP_CTRL_CODE[7] VSS net1 hgu_sw_cap DELAY_CAP=DELAY_CAP
x1[72] CAP_CTRL_CODE[7] VSS net1 hgu_sw_cap DELAY_CAP=DELAY_CAP
x1[71] CAP_CTRL_CODE[7] VSS net1 hgu_sw_cap DELAY_CAP=DELAY_CAP
x1[70] CAP_CTRL_CODE[7] VSS net1 hgu_sw_cap DELAY_CAP=DELAY_CAP
x1[69] CAP_CTRL_CODE[7] VSS net1 hgu_sw_cap DELAY_CAP=DELAY_CAP
x1[68] CAP_CTRL_CODE[7] VSS net1 hgu_sw_cap DELAY_CAP=DELAY_CAP
x1[67] CAP_CTRL_CODE[7] VSS net1 hgu_sw_cap DELAY_CAP=DELAY_CAP
x1[66] CAP_CTRL_CODE[7] VSS net1 hgu_sw_cap DELAY_CAP=DELAY_CAP
x1[65] CAP_CTRL_CODE[7] VSS net1 hgu_sw_cap DELAY_CAP=DELAY_CAP
x1[64] CAP_CTRL_CODE[7] VSS net1 hgu_sw_cap DELAY_CAP=DELAY_CAP
x1[63] CAP_CTRL_CODE[7] VSS net1 hgu_sw_cap DELAY_CAP=DELAY_CAP
x1[62] CAP_CTRL_CODE[7] VSS net1 hgu_sw_cap DELAY_CAP=DELAY_CAP
x1[61] CAP_CTRL_CODE[7] VSS net1 hgu_sw_cap DELAY_CAP=DELAY_CAP
x1[60] CAP_CTRL_CODE[7] VSS net1 hgu_sw_cap DELAY_CAP=DELAY_CAP
x1[59] CAP_CTRL_CODE[7] VSS net1 hgu_sw_cap DELAY_CAP=DELAY_CAP
x1[58] CAP_CTRL_CODE[7] VSS net1 hgu_sw_cap DELAY_CAP=DELAY_CAP
x1[57] CAP_CTRL_CODE[7] VSS net1 hgu_sw_cap DELAY_CAP=DELAY_CAP
x1[56] CAP_CTRL_CODE[7] VSS net1 hgu_sw_cap DELAY_CAP=DELAY_CAP
x1[55] CAP_CTRL_CODE[7] VSS net1 hgu_sw_cap DELAY_CAP=DELAY_CAP
x1[54] CAP_CTRL_CODE[7] VSS net1 hgu_sw_cap DELAY_CAP=DELAY_CAP
x1[53] CAP_CTRL_CODE[7] VSS net1 hgu_sw_cap DELAY_CAP=DELAY_CAP
x1[52] CAP_CTRL_CODE[7] VSS net1 hgu_sw_cap DELAY_CAP=DELAY_CAP
x1[51] CAP_CTRL_CODE[7] VSS net1 hgu_sw_cap DELAY_CAP=DELAY_CAP
x1[50] CAP_CTRL_CODE[7] VSS net1 hgu_sw_cap DELAY_CAP=DELAY_CAP
x1[49] CAP_CTRL_CODE[7] VSS net1 hgu_sw_cap DELAY_CAP=DELAY_CAP
x1[48] CAP_CTRL_CODE[7] VSS net1 hgu_sw_cap DELAY_CAP=DELAY_CAP
x1[47] CAP_CTRL_CODE[7] VSS net1 hgu_sw_cap DELAY_CAP=DELAY_CAP
x1[46] CAP_CTRL_CODE[7] VSS net1 hgu_sw_cap DELAY_CAP=DELAY_CAP
x1[45] CAP_CTRL_CODE[7] VSS net1 hgu_sw_cap DELAY_CAP=DELAY_CAP
x1[44] CAP_CTRL_CODE[7] VSS net1 hgu_sw_cap DELAY_CAP=DELAY_CAP
x1[43] CAP_CTRL_CODE[7] VSS net1 hgu_sw_cap DELAY_CAP=DELAY_CAP
x1[42] CAP_CTRL_CODE[7] VSS net1 hgu_sw_cap DELAY_CAP=DELAY_CAP
x1[41] CAP_CTRL_CODE[7] VSS net1 hgu_sw_cap DELAY_CAP=DELAY_CAP
x1[40] CAP_CTRL_CODE[7] VSS net1 hgu_sw_cap DELAY_CAP=DELAY_CAP
x1[39] CAP_CTRL_CODE[7] VSS net1 hgu_sw_cap DELAY_CAP=DELAY_CAP
x1[38] CAP_CTRL_CODE[7] VSS net1 hgu_sw_cap DELAY_CAP=DELAY_CAP
x1[37] CAP_CTRL_CODE[7] VSS net1 hgu_sw_cap DELAY_CAP=DELAY_CAP
x1[36] CAP_CTRL_CODE[7] VSS net1 hgu_sw_cap DELAY_CAP=DELAY_CAP
x1[35] CAP_CTRL_CODE[7] VSS net1 hgu_sw_cap DELAY_CAP=DELAY_CAP
x1[34] CAP_CTRL_CODE[7] VSS net1 hgu_sw_cap DELAY_CAP=DELAY_CAP
x1[33] CAP_CTRL_CODE[7] VSS net1 hgu_sw_cap DELAY_CAP=DELAY_CAP
x1[32] CAP_CTRL_CODE[7] VSS net1 hgu_sw_cap DELAY_CAP=DELAY_CAP
x1[31] CAP_CTRL_CODE[7] VSS net1 hgu_sw_cap DELAY_CAP=DELAY_CAP
x1[30] CAP_CTRL_CODE[7] VSS net1 hgu_sw_cap DELAY_CAP=DELAY_CAP
x1[29] CAP_CTRL_CODE[7] VSS net1 hgu_sw_cap DELAY_CAP=DELAY_CAP
x1[28] CAP_CTRL_CODE[7] VSS net1 hgu_sw_cap DELAY_CAP=DELAY_CAP
x1[27] CAP_CTRL_CODE[7] VSS net1 hgu_sw_cap DELAY_CAP=DELAY_CAP
x1[26] CAP_CTRL_CODE[7] VSS net1 hgu_sw_cap DELAY_CAP=DELAY_CAP
x1[25] CAP_CTRL_CODE[7] VSS net1 hgu_sw_cap DELAY_CAP=DELAY_CAP
x1[24] CAP_CTRL_CODE[7] VSS net1 hgu_sw_cap DELAY_CAP=DELAY_CAP
x1[23] CAP_CTRL_CODE[7] VSS net1 hgu_sw_cap DELAY_CAP=DELAY_CAP
x1[22] CAP_CTRL_CODE[7] VSS net1 hgu_sw_cap DELAY_CAP=DELAY_CAP
x1[21] CAP_CTRL_CODE[7] VSS net1 hgu_sw_cap DELAY_CAP=DELAY_CAP
x1[20] CAP_CTRL_CODE[7] VSS net1 hgu_sw_cap DELAY_CAP=DELAY_CAP
x1[19] CAP_CTRL_CODE[7] VSS net1 hgu_sw_cap DELAY_CAP=DELAY_CAP
x1[18] CAP_CTRL_CODE[7] VSS net1 hgu_sw_cap DELAY_CAP=DELAY_CAP
x1[17] CAP_CTRL_CODE[7] VSS net1 hgu_sw_cap DELAY_CAP=DELAY_CAP
x1[16] CAP_CTRL_CODE[7] VSS net1 hgu_sw_cap DELAY_CAP=DELAY_CAP
x1[15] CAP_CTRL_CODE[7] VSS net1 hgu_sw_cap DELAY_CAP=DELAY_CAP
x1[14] CAP_CTRL_CODE[7] VSS net1 hgu_sw_cap DELAY_CAP=DELAY_CAP
x1[13] CAP_CTRL_CODE[7] VSS net1 hgu_sw_cap DELAY_CAP=DELAY_CAP
x1[12] CAP_CTRL_CODE[7] VSS net1 hgu_sw_cap DELAY_CAP=DELAY_CAP
x1[11] CAP_CTRL_CODE[7] VSS net1 hgu_sw_cap DELAY_CAP=DELAY_CAP
x1[10] CAP_CTRL_CODE[7] VSS net1 hgu_sw_cap DELAY_CAP=DELAY_CAP
x1[9] CAP_CTRL_CODE[7] VSS net1 hgu_sw_cap DELAY_CAP=DELAY_CAP
x1[8] CAP_CTRL_CODE[7] VSS net1 hgu_sw_cap DELAY_CAP=DELAY_CAP
x1[7] CAP_CTRL_CODE[7] VSS net1 hgu_sw_cap DELAY_CAP=DELAY_CAP
x1[6] CAP_CTRL_CODE[7] VSS net1 hgu_sw_cap DELAY_CAP=DELAY_CAP
x1[5] CAP_CTRL_CODE[7] VSS net1 hgu_sw_cap DELAY_CAP=DELAY_CAP
x1[4] CAP_CTRL_CODE[7] VSS net1 hgu_sw_cap DELAY_CAP=DELAY_CAP
x1[3] CAP_CTRL_CODE[7] VSS net1 hgu_sw_cap DELAY_CAP=DELAY_CAP
x1[2] CAP_CTRL_CODE[7] VSS net1 hgu_sw_cap DELAY_CAP=DELAY_CAP
x1[1] CAP_CTRL_CODE[7] VSS net1 hgu_sw_cap DELAY_CAP=DELAY_CAP
x1[0] CAP_CTRL_CODE[7] VSS net1 hgu_sw_cap DELAY_CAP=DELAY_CAP
.ends


* expanding   symbol:  ../xschem/hgu_sw_cap.sym # of pins=3
** sym_path: hgu/xschem/hgu_sw_cap.sym
** sch_path: hgu/xschem/hgu_sw_cap.sch
.subckt hgu_sw_cap SW VSS DELAY_SIGNAL  DELAY_CAP=DELAY_CAP
*.ipin SW
*.ipin VSS
*.iopin DELAY_SIGNAL
XM14 DELAY_SIGNAL SW net1 VSS sky130_fd_pr__nfet_01v8 L=0.15 W=0.42 nf=1 ad='int((nf+1)/2) * W/nf * 0.29'
+ as='int((nf+2)/2) * W/nf * 0.29' pd='2*int((nf+1)/2) * (W/nf + 0.29)' ps='2*int((nf+2)/2) * (W/nf + 0.29)'
+ nrd='0.29 / W' nrs='0.29 / W' sa=0 sb=0 sd=0 mult=1 m=1
C1 net1 VSS 4.37f m=1
.ends

.GLOBAL GND
.GLOBAL VDD
.GLOBAL cap_ctrl_code[7]
.GLOBAL cap_ctrl_code[6]
.GLOBAL cap_ctrl_code[5]
.GLOBAL cap_ctrl_code[4]
.GLOBAL cap_ctrl_code[3]
.GLOBAL cap_ctrl_code[2]
.GLOBAL cap_ctrl_code[1]
.GLOBAL cap_ctrl_code[0]
.GLOBAL VGND
.GLOBAL VNB
.GLOBAL VPB
.GLOBAL VPWR
.end
